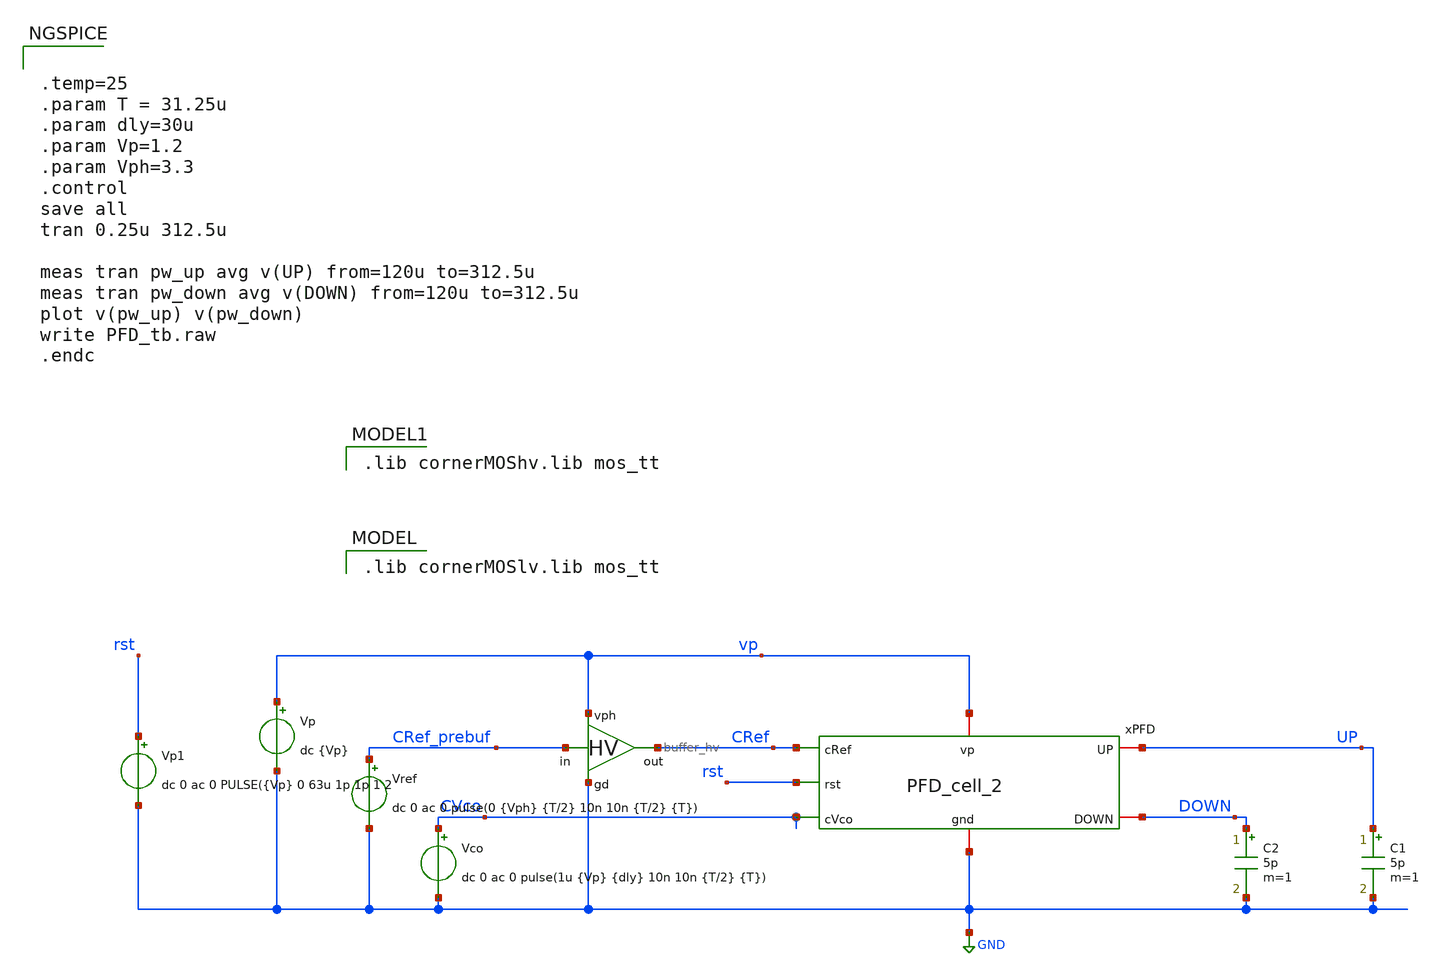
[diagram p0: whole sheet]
** sch_path: schematics/PFD/PFD_tb.sch
**.subckt PFD_tb
Vref CRef_prebuf GND dc 0 ac 0 pulse(0 {Vph} {T/2} 10n 10n {T/2} {T})
Vco CVco GND dc 0 ac 0 pulse(1u {Vp} {dly} 10n 10n {T/2} {T})
Vp vp GND dc {Vp}
C1 UP GND 5p m=1
C2 DOWN GND 5p m=1
xPFD GND vp CRef UP DOWN CVco rst PFD_cell_2
x2 vp CRef_prebuf CRef GND buffer_hv
Vp1 rst GND dc 0 ac 0 PULSE({Vp} 0 63u 1p 1p 1 2
**** begin user architecture code
 .lib cornerMOSlv.lib mos_tt



.temp=25
.param T = 31.25u
.param dly=30u
.param Vp=1.2
.param Vph=3.3
.control
save all
tran 0.25u 312.5u

meas tran pw_up avg v(UP) from=120u to=312.5u
meas tran pw_down avg v(DOWN) from=120u to=312.5u
plot v(pw_up) v(pw_down)
write PFD_tb.raw
.endc


 .lib cornerMOShv.lib mos_tt

**** end user architecture code
**.ends
.GLOBAL GND
.end
